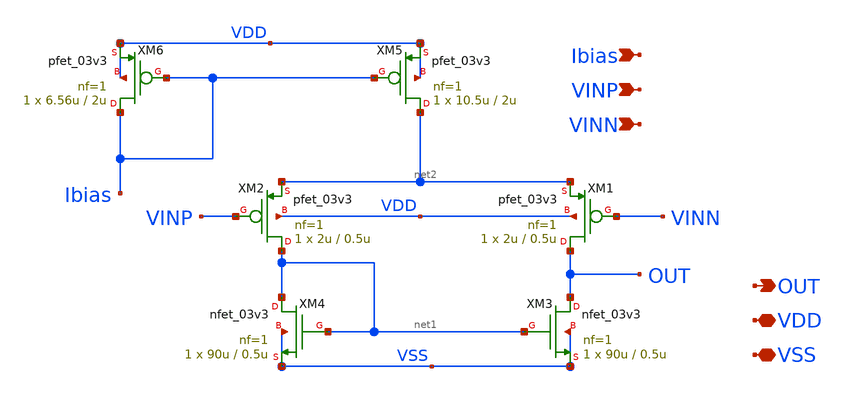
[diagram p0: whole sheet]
** sch_path: pmos-ota/pmos-5t-ota.sch
**.subckt pmos-5t-ota Ibias VINP VINN OUT VDD VSS
*.ipin Ibias
*.ipin VINP
*.ipin VINN
*.opin OUT
*.iopin VDD
*.iopin VSS
XM1 OUT VINN net2 VDD pfet_03v3 L=0.5u W=2u nf=1 ad='int((nf+1)/2) * W/nf * 0.18u' as='int((nf+2)/2) * W/nf * 0.18u'
+ pd='2*int((nf+1)/2) * (W/nf + 0.18u)' ps='2*int((nf+2)/2) * (W/nf + 0.18u)' nrd='0.18u / W' nrs='0.18u / W'
+ sa=0 sb=0 sd=0 m=1
XM2 net1 VINP net2 VDD pfet_03v3 L=0.5u W=2u nf=1 ad='int((nf+1)/2) * W/nf * 0.18u' as='int((nf+2)/2) * W/nf * 0.18u'
+ pd='2*int((nf+1)/2) * (W/nf + 0.18u)' ps='2*int((nf+2)/2) * (W/nf + 0.18u)' nrd='0.18u / W' nrs='0.18u / W'
+ sa=0 sb=0 sd=0 m=1
XM3 OUT net1 VSS VSS nfet_03v3 L=0.5u W=90u nf=1 ad='int((nf+1)/2) * W/nf * 0.18u' as='int((nf+2)/2) * W/nf * 0.18u'
+ pd='2*int((nf+1)/2) * (W/nf + 0.18u)' ps='2*int((nf+2)/2) * (W/nf + 0.18u)' nrd='0.18u / W' nrs='0.18u / W'
+ sa=0 sb=0 sd=0 m=1
XM4 net1 net1 VSS VSS nfet_03v3 L=0.5u W=90u nf=1 ad='int((nf+1)/2) * W/nf * 0.18u' as='int((nf+2)/2) * W/nf * 0.18u'
+ pd='2*int((nf+1)/2) * (W/nf + 0.18u)' ps='2*int((nf+2)/2) * (W/nf + 0.18u)' nrd='0.18u / W' nrs='0.18u / W'
+ sa=0 sb=0 sd=0 m=1
XM5 net2 Ibias VDD VDD pfet_03v3 L=2u W=10.5u nf=1 ad='int((nf+1)/2) * W/nf * 0.18u' as='int((nf+2)/2) * W/nf * 0.18u'
+ pd='2*int((nf+1)/2) * (W/nf + 0.18u)' ps='2*int((nf+2)/2) * (W/nf + 0.18u)' nrd='0.18u / W' nrs='0.18u / W'
+ sa=0 sb=0 sd=0 m=1
XM6 Ibias Ibias VDD VDD pfet_03v3 L=2u W=6.56u nf=1 ad='int((nf+1)/2) * W/nf * 0.18u' as='int((nf+2)/2) * W/nf * 0.18u'
+ pd='2*int((nf+1)/2) * (W/nf + 0.18u)' ps='2*int((nf+2)/2) * (W/nf + 0.18u)' nrd='0.18u / W' nrs='0.18u / W'
+ sa=0 sb=0 sd=0 m=1
**.ends
.end
